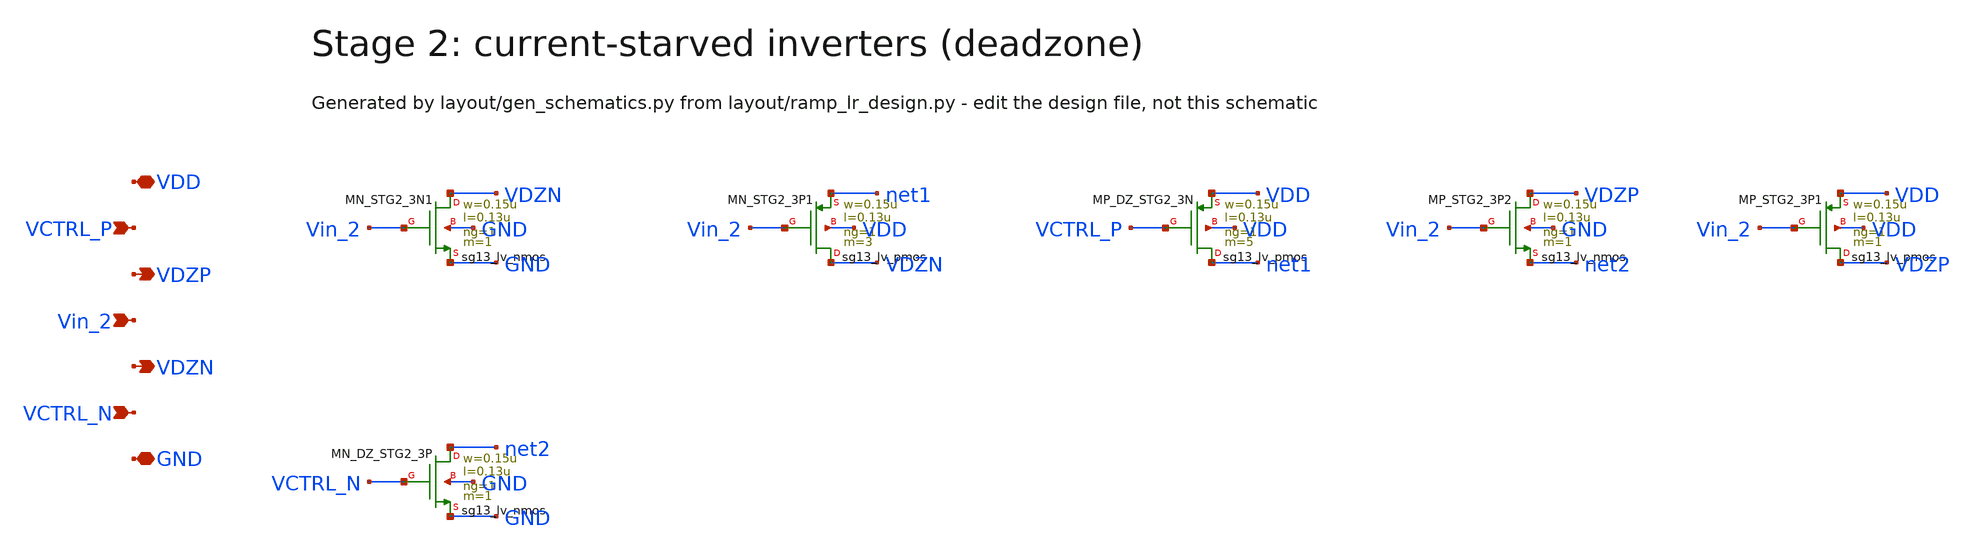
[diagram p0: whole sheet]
** sch_path: Design Files/RAMP/RAMP-LR/STG2_LR.sch
**.subckt STG2_LR VDD VCTRL_P VDZP Vin_2 VDZN VCTRL_N GND
*.iopin VDD
*.ipin VCTRL_P
*.opin VDZP
*.ipin Vin_2
*.opin VDZN
*.ipin VCTRL_N
*.iopin GND
XMN_STG2_3N1 VDZN Vin_2 GND GND sg13_lv_nmos w=0.15u l=0.13u ng=1 m=1 mm_ok=1
XMN_STG2_3P1 VDZN Vin_2 net1 VDD sg13_lv_pmos w=0.15u l=0.13u ng=1 m=3 mm_ok=1
XMP_DZ_STG2_3N net1 VCTRL_P VDD VDD sg13_lv_pmos w=0.15u l=0.13u ng=1 m=5 mm_ok=1
XMP_STG2_3P2 VDZP Vin_2 net2 GND sg13_lv_nmos w=0.15u l=0.13u ng=1 m=1 mm_ok=1
XMP_STG2_3P1 VDZP Vin_2 VDD VDD sg13_lv_pmos w=0.15u l=0.13u ng=1 m=1 mm_ok=1
XMN_DZ_STG2_3P net2 VCTRL_N GND GND sg13_lv_nmos w=0.15u l=0.13u ng=1 m=1 mm_ok=1
**.ends
.end
